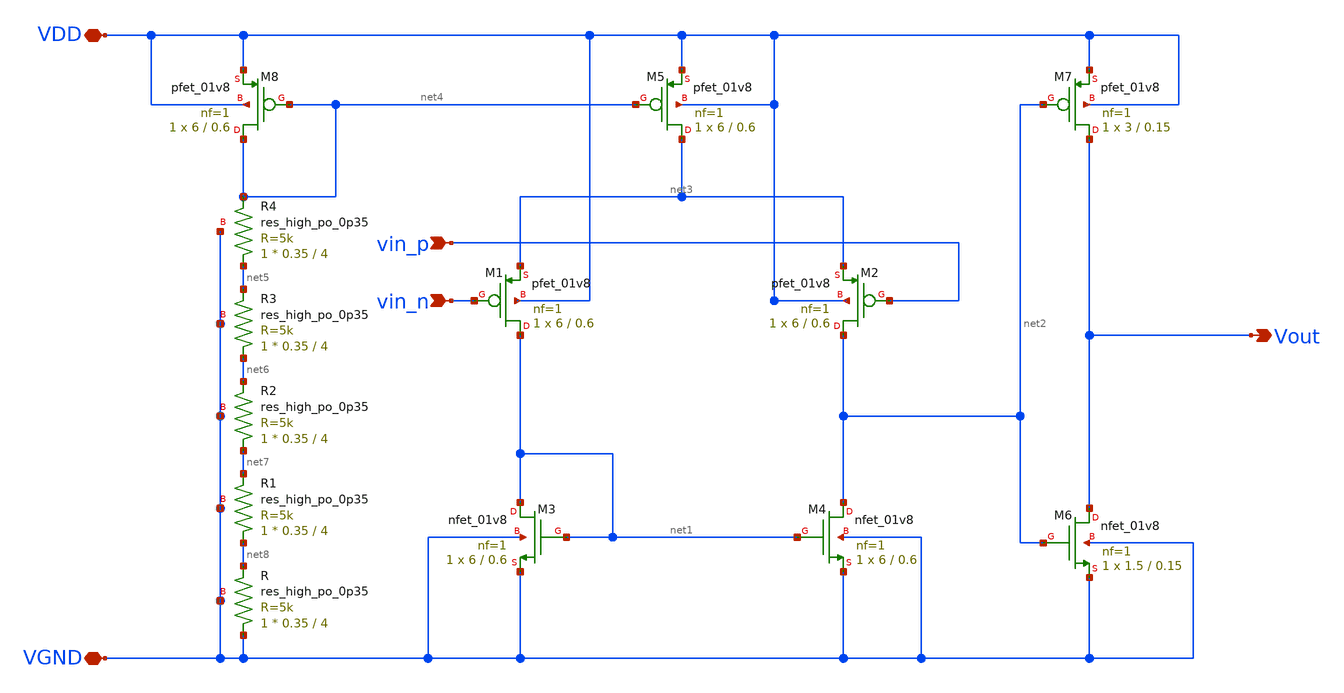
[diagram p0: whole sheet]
** sch_path: xschem/opamp.sch
**.subckt opamp vin_n vin_p Vout VDD VGND
*.ipin vin_n
*.ipin vin_p
*.opin Vout
*.iopin VDD
*.iopin VGND
XM1 net1 vin_n net3 VDD sky130_fd_pr__pfet_01v8 L=0.6 W=6 nf=1 ad='W * 0.29' as='W * 0.29' pd='2 * (W + 0.29)'
+ ps='2 * (W + 0.29)' nrd='0.29 / W' nrs='0.29 / W' sa=0 sb=0 sd=0 mult=1 m=1
XM2 net2 vin_p net3 VDD sky130_fd_pr__pfet_01v8 L=0.6 W=6 nf=1 ad='W * 0.29' as='W * 0.29' pd='2 * (W + 0.29)'
+ ps='2 * (W + 0.29)' nrd='0.29 / W' nrs='0.29 / W' sa=0 sb=0 sd=0 mult=1 m=1
XM3 net1 net1 VGND VGND sky130_fd_pr__nfet_01v8 L=0.6 W=6 nf=1 ad='W * 0.29' as='W * 0.29' pd='2 * (W + 0.29)'
+ ps='2 * (W + 0.29)' nrd='0.29 / W' nrs='0.29 / W' sa=0 sb=0 sd=0 mult=1 m=1
XM4 net2 net1 VGND VGND sky130_fd_pr__nfet_01v8 L=0.6 W=6 nf=1 ad='W * 0.29' as='W * 0.29' pd='2 * (W + 0.29)'
+ ps='2 * (W + 0.29)' nrd='0.29 / W' nrs='0.29 / W' sa=0 sb=0 sd=0 mult=1 m=1
XM5 net3 net4 VDD VDD sky130_fd_pr__pfet_01v8 L=0.6 W=6 nf=1 ad='W * 0.29' as='W * 0.29' pd='2 * (W + 0.29)'
+ ps='2 * (W + 0.29)' nrd='0.29 / W' nrs='0.29 / W' sa=0 sb=0 sd=0 mult=1 m=1
XM7 Vout net2 VDD VDD sky130_fd_pr__pfet_01v8 L=0.15 W=3 nf=1 ad='W * 0.29' as='W * 0.29' pd='2 * (W + 0.29)'
+ ps='2 * (W + 0.29)' nrd='0.29 / W' nrs='0.29 / W' sa=0 sb=0 sd=0 mult=1 m=1
XM8 net4 net4 VDD VDD sky130_fd_pr__pfet_01v8 L=0.6 W=6 nf=1 ad='W * 0.29' as='W * 0.29' pd='2 * (W + 0.29)'
+ ps='2 * (W + 0.29)' nrd='0.29 / W' nrs='0.29 / W' sa=0 sb=0 sd=0 mult=1 m=1
XM6 Vout net2 VGND VGND sky130_fd_pr__nfet_01v8 L=0.15 W=1.5 nf=1 ad='W * 0.29' as='W * 0.29' pd='2 * (W + 0.29)'
+ ps='2 * (W + 0.29)' nrd='0.29 / W' nrs='0.29 / W' sa=0 sb=0 sd=0 mult=1 m=1
XR VGND net8 VGND sky130_fd_pr__res_high_po_0p35 L=4 mult=1 m=1
XR1 net8 net7 VGND sky130_fd_pr__res_high_po_0p35 L=4 mult=1 m=1
XR2 net7 net6 VGND sky130_fd_pr__res_high_po_0p35 L=4 mult=1 m=1
XR3 net6 net5 VGND sky130_fd_pr__res_high_po_0p35 L=4 mult=1 m=1
XR4 net5 net4 VGND sky130_fd_pr__res_high_po_0p35 L=4 mult=1 m=1
**.ends
.end
